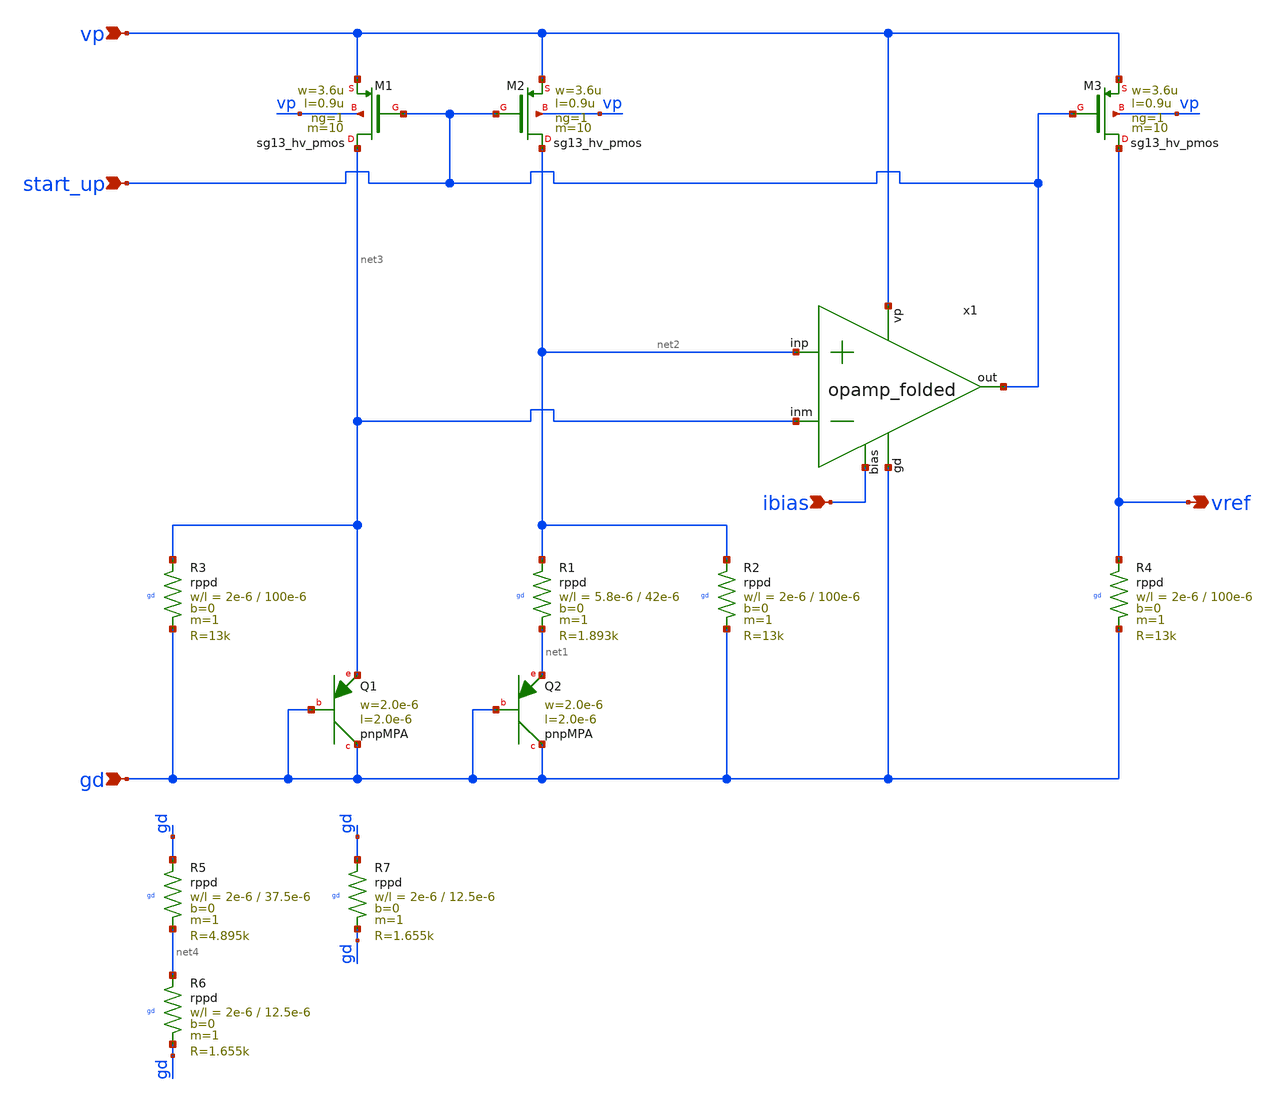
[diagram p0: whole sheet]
** sch_path: PLL0663-main/schematic/xschem/bandgap/bandgap_res_core_full.sch
**.subckt bandgap_res_core_full gd vp ibias vref start_up
*.ipin gd
*.ipin vp
*.ipin ibias
*.opin vref
*.ipin start_up
XQ1 gd gd net3 pnpMPA a=4p p=8u m=1
XQ2 gd gd net1 pnpMPA a=4p p=8u m=8
XM2 net2 start_up vp vp sg13_hv_pmos w=3.6u l=0.9u ng=1 m=10 mm_ok=1
XM1 net3 start_up vp vp sg13_hv_pmos w=3.6u l=0.9u ng=1 m=10 mm_ok=1
XM3 vref start_up vp vp sg13_hv_pmos w=3.6u l=0.9u ng=1 m=10 mm_ok=1
XR2 net2 gd gd rppd w=2e-6 l=100e-6 m=1 b=0 mm_ok=1
XR3 net3 gd gd rppd w=2e-6 l=100e-6 m=1 b=0 mm_ok=1
XR4 vref gd gd rppd w=2e-6 l=100e-6 m=1 b=0 mm_ok=1
XR1 net2 net1 gd rppd w=5.8e-6 l=42e-6 m=1 b=0 mm_ok=1
x1 vp net2 net3 start_up ibias gd opamp_folded
XR5 gd net4 gd rppd w=2e-6 l=37.5e-6 m=1 b=0 mm_ok=1
XR6 net4 gd gd rppd w=2e-6 l=12.5e-6 m=1 b=0 mm_ok=1
XR7 gd gd gd rppd w=2e-6 l=12.5e-6 m=1 b=0 mm_ok=1
**.ends
.end
